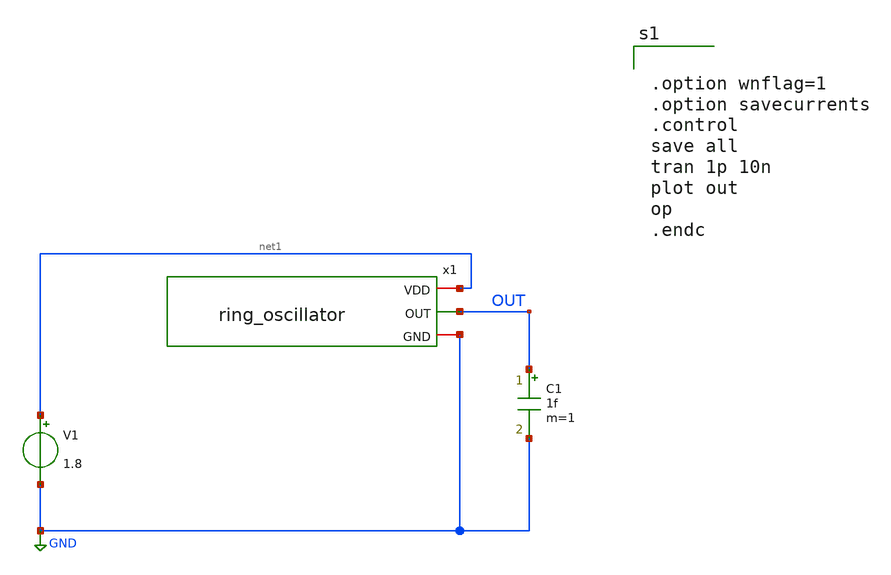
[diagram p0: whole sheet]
** sch_path: schematics/Layouting/ring_oscillator_tb.sch
**.subckt ring_oscillator_tb
V1 net1 GND 1.8
C1 OUT GND 1f m=1
x1 net1 OUT GND ring_oscillator
**** begin user architecture code


.option wnflag=1
.option savecurrents
.control
save all
tran 1p 10n
plot out
op
.endc


 .lib $::SKYWATER_MODELS/sky130.lib.spice tt
.param mc_mmm_cwitch=0
.param mc_pr_switch=1

**** end user architecture code
**.ends

* expanding   symbol:  /home/raditya/Silicons/Projects/ring_oscillator.sym # of pins=3
** sym_path: schematics/Layouting/ring_oscillator.sym
** sch_path: schematics/Layouting/ring_oscillator.sch
.subckt ring_oscillator VDD OUT GND
*.iopin VDD
*.iopin GND
*.opin OUT
x1 VDD net2 net3 GND inverter_symbol
x2 VDD net3 net4 GND inverter_symbol
x3 VDD net1 net2 GND inverter_symbol
x4 VDD net4 OUT GND inverter_symbol
x5 VDD OUT net1 GND inverter_symbol
.ends


* expanding   symbol:  /home/raditya/Silicons/Projects/inverter_symbol.sym # of pins=4
** sym_path: schematics/Layouting/inverter_symbol.sym
** sch_path: schematics/Layouting/inverter_symbol.sch
.subckt inverter_symbol VDD In Out GND
*.ipin In
*.opin Out
*.iopin VDD
*.iopin GND
XM9 Out In GND GND sky130_fd_pr__nfet_01v8 L=0.15 W=1 nf=1 ad='int((nf+1)/2) * W/nf * 0.29' as='int((nf+2)/2) * W/nf * 0.29'
+ pd='2*int((nf+1)/2) * (W/nf + 0.29)' ps='2*int((nf+2)/2) * (W/nf + 0.29)' nrd='0.29 / W' nrs='0.29 / W'
+ sa=0 sb=0 sd=0 mult=1 m=1
XM10 Out In VDD VDD sky130_fd_pr__pfet_01v8 L=0.15 W=1 nf=1 ad='int((nf+1)/2) * W/nf * 0.29' as='int((nf+2)/2) * W/nf * 0.29'
+ pd='2*int((nf+1)/2) * (W/nf + 0.29)' ps='2*int((nf+2)/2) * (W/nf + 0.29)' nrd='0.29 / W' nrs='0.29 / W'
+ sa=0 sb=0 sd=0 mult=1 m=1
.ends

.GLOBAL GND
.end
